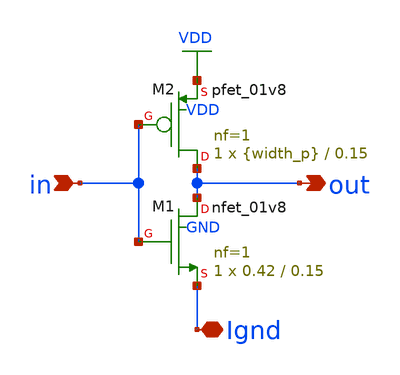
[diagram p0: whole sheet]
** sch_path: tutorial-3/source/inv_gnd.sch
**.subckt inv_gnd in out Ignd
*.ipin in
*.opin out
*.iopin Ignd
XM1 out in Ignd GND sky130_fd_pr__nfet_01v8 L=0.15 W=0.42 nf=1 ad='int((nf+1)/2) * W/nf * 0.29' as='int((nf+2)/2) * W/nf * 0.29'
+ pd='2*int((nf+1)/2) * (W/nf + 0.29)' ps='2*int((nf+2)/2) * (W/nf + 0.29)' nrd='0.29 / W' nrs='0.29 / W'
+ sa=0 sb=0 sd=0 mult=1 m=1
XM2 out in VDD VDD sky130_fd_pr__pfet_01v8 L=0.15 W={width_p} nf=1 ad='int((nf+1)/2) * W/nf * 0.29' as='int((nf+2)/2) * W/nf * 0.29'
+ pd='2*int((nf+1)/2) * (W/nf + 0.29)' ps='2*int((nf+2)/2) * (W/nf + 0.29)' nrd='0.29 / W' nrs='0.29 / W'
+ sa=0 sb=0 sd=0 mult=1 m=1
**.ends
.GLOBAL VDD
.end
